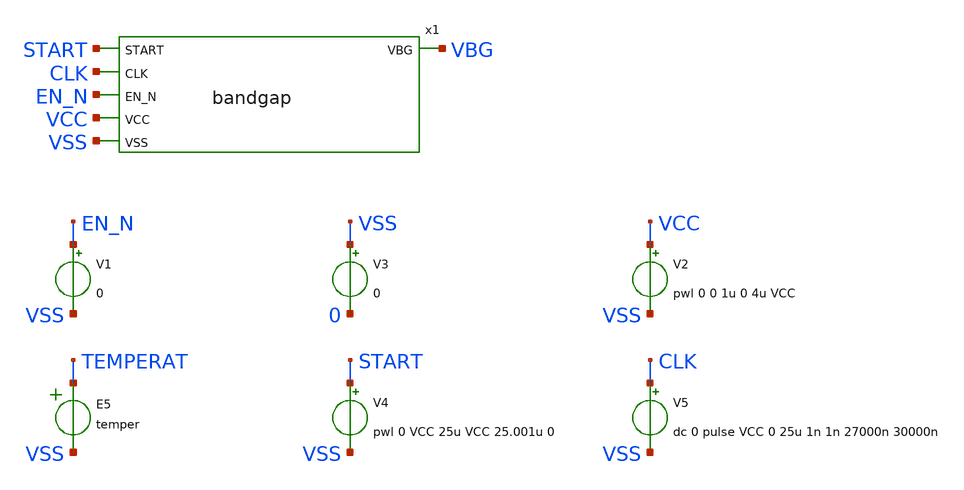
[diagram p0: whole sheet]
** sch_path: sky130_tests/tb_bandgap.sch
* Copyright 2020 Stefan Frederik Schippers
* Licensed under the Apache License, Version 2.0 (the "License");
* you may not use this file except in compliance with the License.
* You may obtain a copy of the License at
* https://www.apache.org/licenses/LICENSE-2.0
* Unless required by applicable law or agreed to in writing, software
* distributed under the License is distributed on an "AS IS" BASIS,
* WITHOUT WARRANTIES OR CONDITIONS OF ANY KIND, either express or implied.
* See the License for the specific language governing permissions and
* limitations under the License.
**.subckt tb_bandgap
x1 START CLK EN_N VBG VCC VSS bandgap
V1 EN_N VSS 0
V2 VCC VSS pwl 0 0 1u 0 4u VCC
V3 VSS 0 0
E5 TEMPERAT VSS VOL=' temper '
V4 START VSS pwl 0 VCC 25u VCC 25.001u 0
V5 CLK VSS dc 0 pulse VCC 0 25u 1n 1n 27000n 30000n
**** begin user architecture code

.option seed=13

* this experimental option enables mos model bin
* selection based on W/NF instead of W
.options wnflag=1 XMU=0.49 METHOD=GEAR ITL4=100 CHGTOL=1e-15 TRTOL=1 RELTOL=0.0001 VNTOL=0.1u
.param ABSVAR=0.03
.param VCCGAUSS=agauss(1.8, 'ABSVAR', 1)
.param VCC=VCCGAUSS
* .param VCC=1.8
** variation marameters:
.param sky130_fd_pr__nfet_01v8_lvt__vth0_slope_spectre='agauss(0, ABSVAR, 3)/sky130_fd_pr__nfet_01v8_lvt__vth0_slope'
.param sky130_fd_pr__pfet_01v8_lvt__vth0_slope_spectre='agauss(0, ABSVAR, 3)/sky130_fd_pr__pfet_01v8_lvt__vth0_slope'
.param sky130_fd_pr__nfet_01v8__vth0_slope_spectre='agauss(0, ABSVAR, 3)/sky130_fd_pr__nfet_01v8__vth0_slope'
.param sky130_fd_pr__pfet_01v8__vth0_slope_spectre='agauss(0, ABSVAR, 3)/sky130_fd_pr__pfet_01v8__vth0_slope'

.param sky130_fd_pr__pfet_01v8__toxe_slope_spectre='agauss(0, ABSVAR*2, 3)/sky130_fd_pr__pfet_01v8__toxe_slope'
.param sky130_fd_pr__nfet_01v8__toxe_slope_spectre='agauss(0, ABSVAR*2, 3)/sky130_fd_pr__nfet_01v8__toxe_slope'
.param sky130_fd_pr__pfet_01v8_lvt__toxe_slope_spectre='agauss(0, ABSVAR*2, 3)/sky130_fd_pr__pfet_01v8_lvt__toxe_slope'
.param sky130_fd_pr__nfet_01v8_lvt__toxe_slope_spectre='agauss(0, ABSVAR*2, 3)/sky130_fd_pr__nfet_01v8_lvt__toxe_slope'

.param sky130_fd_pr__res_high_po__var_mult=agauss(0, 'ABSVAR*8', 1)

* .options savecurrents
.control
  let run=1
  dowhile run <= 40
    if run > 1
      reset
      set appendwrite
    end
    * save vbg x1.plus x1.minus i(v2) vcc
    save all
    if run % 3 = 0
      set temp=-40
    end
    if run % 3 = 1
      set temp=27
    end
    if run % 3 = 2
      set temp=125
    end
    tran 0.05u 150u
    write tb_bandgap.raw
    let run = run + 1
  end
  set nolegend
  plot all.vbg
.endc


 ** manual skywater pdks install (with patches applied)
* .lib $::SKYWATER_MODELS/models/sky130.lib.spice tt

** opencircuitdesign pdks install
.lib $::SKYWATER_MODELS/sky130.lib.spice tt

.param mc_mm_switch=0
.param mc_pr_switch=0

**** end user architecture code
**.ends
.end
